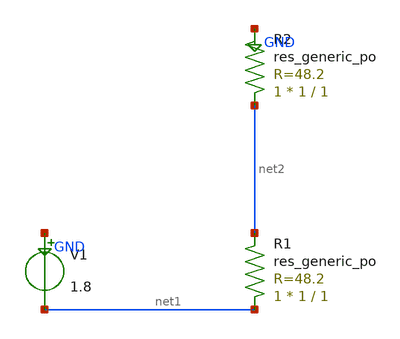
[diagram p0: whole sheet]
** sch_path: design/smoke_test.sch
**.subckt smoke_test
V1 GND net1 1.8
XR1 net1 net2 sky130_fd_pr__res_generic_po W=1 L=1 m=1
XR2 net2 GND sky130_fd_pr__res_generic_po W=1 L=1 m=1
**** begin user architecture code

** sky130 PDK model include (tt corner) — see docs/environment-setup.md
.lib $::SKYWATER_MODELS/sky130.lib.spice tt
.op

**** end user architecture code
**.ends
.GLOBAL GND
.end
